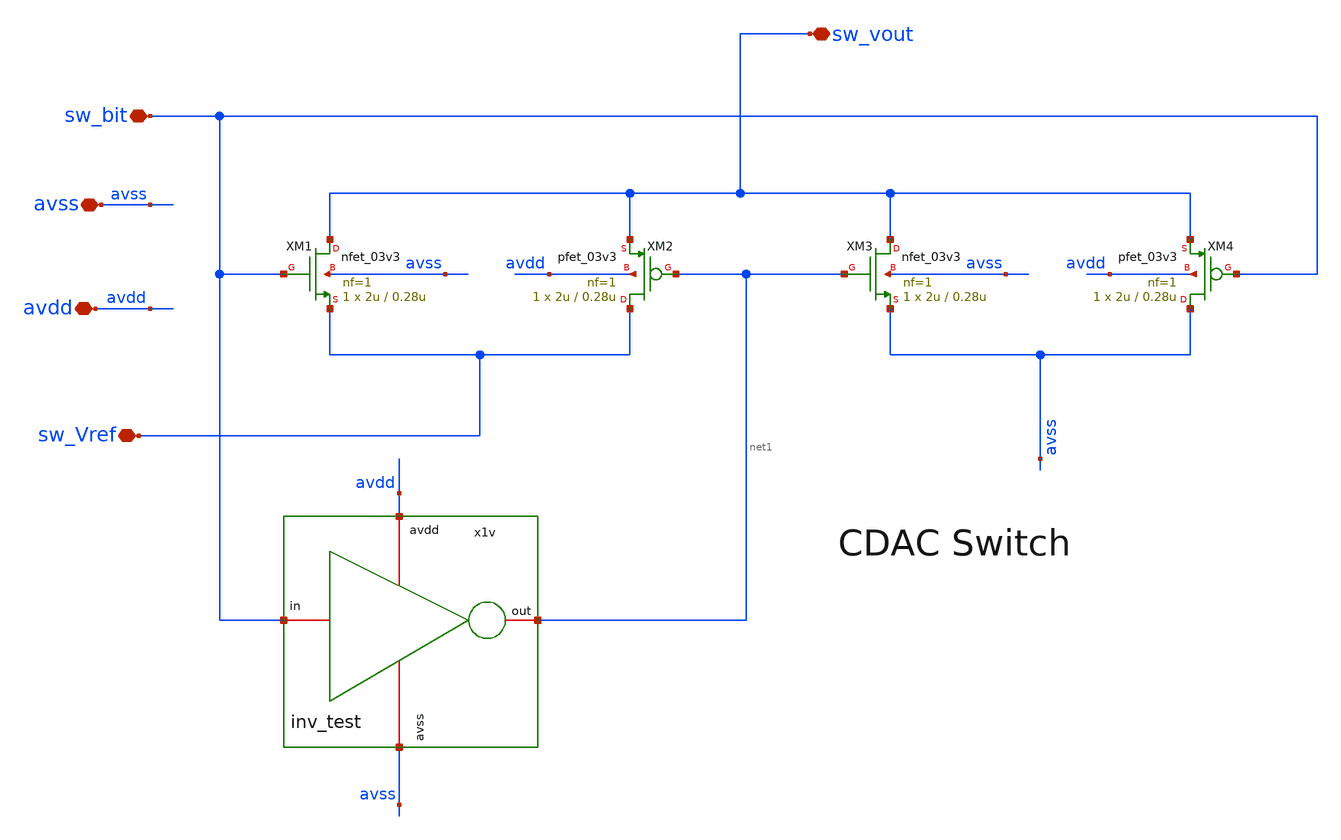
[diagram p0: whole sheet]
** sch_path: designs/libs/WK_Kadam/c_dac1_switch.sch
**.subckt c_dac1_switch avdd avss sw_bit sw_vout sw_Vref
*.iopin avdd
*.iopin avss
*.iopin sw_bit
*.iopin sw_vout
*.iopin sw_Vref
XM1 sw_vout sw_bit sw_Vref avss nfet_03v3 L=0.28u W=2u nf=1 ad='int((nf+1)/2) * W/nf * 0.18u' as='int((nf+2)/2) * W/nf * 0.18u'
+ pd='2*int((nf+1)/2) * (W/nf + 0.18u)' ps='2*int((nf+2)/2) * (W/nf + 0.18u)' nrd='0.18u / W' nrs='0.18u / W'
+ sa=0 sb=0 sd=0 m=1
XM3 sw_vout net1 avss avss nfet_03v3 L=0.28u W=2u nf=1 ad='int((nf+1)/2) * W/nf * 0.18u' as='int((nf+2)/2) * W/nf * 0.18u'
+ pd='2*int((nf+1)/2) * (W/nf + 0.18u)' ps='2*int((nf+2)/2) * (W/nf + 0.18u)' nrd='0.18u / W' nrs='0.18u / W'
+ sa=0 sb=0 sd=0 m=1
XM4 avss sw_bit sw_vout avdd pfet_03v3 L=0.28u W=2u nf=1 ad='int((nf+1)/2) * W/nf * 0.18u' as='int((nf+2)/2) * W/nf * 0.18u'
+ pd='2*int((nf+1)/2) * (W/nf + 0.18u)' ps='2*int((nf+2)/2) * (W/nf + 0.18u)' nrd='0.18u / W' nrs='0.18u / W'
+ sa=0 sb=0 sd=0 m=1
XM2 sw_Vref net1 sw_vout avdd pfet_03v3 L=0.28u W=2u nf=1 ad='int((nf+1)/2) * W/nf * 0.18u' as='int((nf+2)/2) * W/nf * 0.18u'
+ pd='2*int((nf+1)/2) * (W/nf + 0.18u)' ps='2*int((nf+2)/2) * (W/nf + 0.18u)' nrd='0.18u / W' nrs='0.18u / W'
+ sa=0 sb=0 sd=0 m=1
x1v avdd sw_bit net1 avss inv_test
**.ends

* expanding   symbol:  Wk_Chip_Odyssey/designs/libs/WK_Kadam/inv_test.sym # of pins=4
** sym_path: Wk_Chip_Odyssey/designs/libs/WK_Kadam/inv_test.sym
** sch_path: Wk_Chip_Odyssey/designs/libs/WK_Kadam/inv_test.sch
.subckt inv_test avdd in out avss
*.iopin avdd
*.iopin avss
*.iopin in
*.iopin out
XM3 out in avss avss nfet_03v3 L=0.28u W=1u nf=1 ad='int((nf+1)/2) * W/nf * 0.18u' as='int((nf+2)/2) * W/nf * 0.18u'
+ pd='2*int((nf+1)/2) * (W/nf + 0.18u)' ps='2*int((nf+2)/2) * (W/nf + 0.18u)' nrd='0.18u / W' nrs='0.18u / W'
+ sa=0 sb=0 sd=0 m=1
XM4 out in avdd avdd pfet_03v3 L=0.28u W=2.5u nf=1 ad='int((nf+1)/2) * W/nf * 0.18u' as='int((nf+2)/2) * W/nf * 0.18u'
+ pd='2*int((nf+1)/2) * (W/nf + 0.18u)' ps='2*int((nf+2)/2) * (W/nf + 0.18u)' nrd='0.18u / W' nrs='0.18u / W'
+ sa=0 sb=0 sd=0 m=1
.ends

.end
